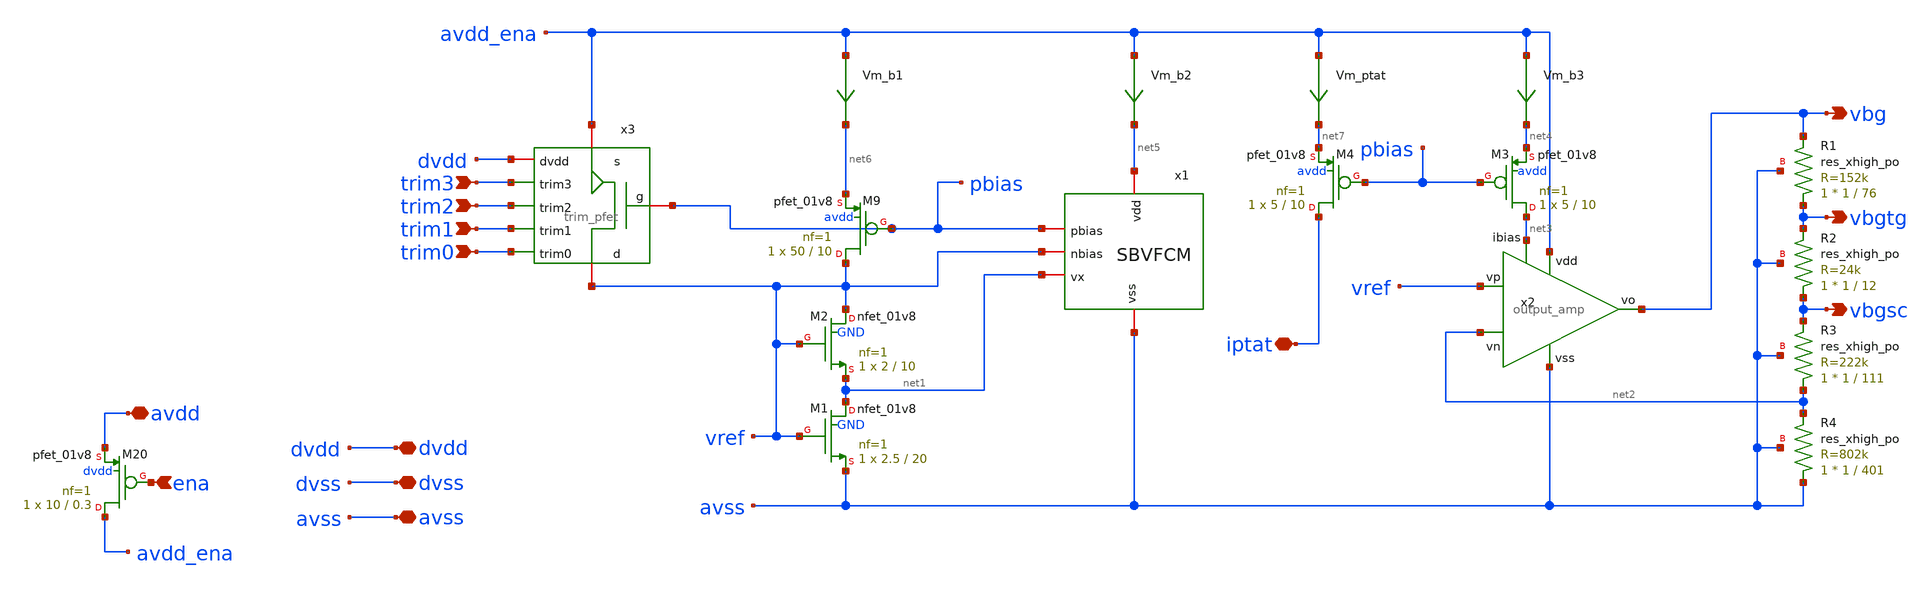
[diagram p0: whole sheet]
** sch_path: xschem/sky130_ak_ip__cmos_vref.sch
**.subckt sky130_ak_ip__cmos_vref vbg avss avdd dvdd dvss ena vbgsc vbgtg trim3 trim2 trim1 trim0
*+ iptat
*.opin vbg
*.iopin avss
*.iopin avdd
*.iopin dvdd
*.iopin dvss
*.ipin ena
*.opin vbgsc
*.opin vbgtg
*.ipin trim3
*.ipin trim2
*.ipin trim1
*.ipin trim0
*.iopin iptat
XM2 vref vref net1 GND sky130_fd_pr__nfet_01v8 L=10 W=2 nf=1 ad='int((nf+1)/2) * W/nf * 0.29' as='int((nf+2)/2) * W/nf * 0.29'
+ pd='2*int((nf+1)/2) * (W/nf + 0.29)' ps='2*int((nf+2)/2) * (W/nf + 0.29)' nrd='0.29 / W' nrs='0.29 / W'
+ sa=0 sb=0 sd=0 mult=1 m=1
XM1 net1 vref avss GND sky130_fd_pr__nfet_01v8 L=20 W=2.5 nf=1 ad='int((nf+1)/2) * W/nf * 0.29' as='int((nf+2)/2) * W/nf * 0.29'
+ pd='2*int((nf+1)/2) * (W/nf + 0.29)' ps='2*int((nf+2)/2) * (W/nf + 0.29)' nrd='0.29 / W' nrs='0.29 / W'
+ sa=0 sb=0 sd=0 mult=1 m=1
XM9 vref pbias net6 avdd sky130_fd_pr__pfet_01v8 L=10 W=50 nf=1 ad='int((nf+1)/2) * W/nf * 0.29' as='int((nf+2)/2) * W/nf * 0.29'
+ pd='2*int((nf+1)/2) * (W/nf + 0.29)' ps='2*int((nf+2)/2) * (W/nf + 0.29)' nrd='0.29 / W' nrs='0.29 / W'
+ sa=0 sb=0 sd=0 mult=1 m=1
XM20 avdd_ena ena avdd dvdd sky130_fd_pr__pfet_01v8 L=0.3 W=10 nf=1 ad='int((nf+1)/2) * W/nf * 0.29'
+ as='int((nf+2)/2) * W/nf * 0.29' pd='2*int((nf+1)/2) * (W/nf + 0.29)' ps='2*int((nf+2)/2) * (W/nf + 0.29)'
+ nrd='0.29 / W' nrs='0.29 / W' sa=0 sb=0 sd=0 mult=1 m=1
x1 net5 pbias vref net1 avss sbvfcm
x2 avdd_ena vbg vref net2 net3 avss output_amp
XM3 net3 pbias net4 avdd sky130_fd_pr__pfet_01v8 L=10 W=5 nf=1 ad='int((nf+1)/2) * W/nf * 0.29' as='int((nf+2)/2) * W/nf * 0.29'
+ pd='2*int((nf+1)/2) * (W/nf + 0.29)' ps='2*int((nf+2)/2) * (W/nf + 0.29)' nrd='0.29 / W' nrs='0.29 / W'
+ sa=0 sb=0 sd=0 mult=1 m=1
Vm_b1 avdd_ena net6 0
.save i(vm_b1)
Vm_b2 avdd_ena net5 0
.save i(vm_b2)
Vm_b3 avdd_ena net4 0
.save i(vm_b3)
x3 dvdd avdd_ena pbias trim0 trim2 trim3 trim1 vref trim_pfet
XM4 iptat pbias net7 avdd sky130_fd_pr__pfet_01v8 L=10 W=5 nf=1 ad='int((nf+1)/2) * W/nf * 0.29' as='int((nf+2)/2) * W/nf * 0.29'
+ pd='2*int((nf+1)/2) * (W/nf + 0.29)' ps='2*int((nf+2)/2) * (W/nf + 0.29)' nrd='0.29 / W' nrs='0.29 / W'
+ sa=0 sb=0 sd=0 mult=1 m=1
Vm_ptat avdd_ena net7 0
.save i(vm_ptat)
XR4 avss net2 avss sky130_fd_pr__res_xhigh_po W=1 L=401 mult=1 m=1
XR3 net2 vbgsc avss sky130_fd_pr__res_xhigh_po W=1 L=111 mult=1 m=1
XR2 vbgsc vbgtg avss sky130_fd_pr__res_xhigh_po W=1 L=12 mult=1 m=1
XR1 vbgtg vbg avss sky130_fd_pr__res_xhigh_po W=1 L=76 mult=1 m=1
**.ends

* expanding   symbol:  /home/moduhub/work/sky130_ak_ip__cmos_vref/xschem/sbvfcm.sym # of pins=5
** sym_path: xschem/sbvfcm.sym
** sch_path: xschem/sbvfcm.sch
.subckt sbvfcm vdd pbias nbias vx vss
*.iopin vss
*.iopin vdd
*.iopin vx
*.iopin pbias
*.iopin nbias
XM3 net1 vbias_st vx GND sky130_fd_pr__nfet_01v8 L=1 W=100 nf=5 ad='int((nf+1)/2) * W/nf * 0.29' as='int((nf+2)/2) * W/nf * 0.29'
+ pd='2*int((nf+1)/2) * (W/nf + 0.29)' ps='2*int((nf+2)/2) * (W/nf + 0.29)' nrd='0.29 / W' nrs='0.29 / W'
+ sa=0 sb=0 sd=0 mult=1 m=1
XM4 net2 vbias_st vss GND sky130_fd_pr__nfet_01v8 L=1 W=5 nf=1 ad='int((nf+1)/2) * W/nf * 0.29' as='int((nf+2)/2) * W/nf * 0.29'
+ pd='2*int((nf+1)/2) * (W/nf + 0.29)' ps='2*int((nf+2)/2) * (W/nf + 0.29)' nrd='0.29 / W' nrs='0.29 / W'
+ sa=0 sb=0 sd=0 mult=1 m=1
XM5 pbias nbias net1 GND sky130_fd_pr__nfet_01v8 L=10 W=10 nf=1 ad='int((nf+1)/2) * W/nf * 0.29' as='int((nf+2)/2) * W/nf * 0.29'
+ pd='2*int((nf+1)/2) * (W/nf + 0.29)' ps='2*int((nf+2)/2) * (W/nf + 0.29)' nrd='0.29 / W' nrs='0.29 / W'
+ sa=0 sb=0 sd=0 mult=1 m=1
XM6 vbias_st nbias net2 GND sky130_fd_pr__nfet_01v8 L=10 W=10 nf=1 ad='int((nf+1)/2) * W/nf * 0.29' as='int((nf+2)/2) * W/nf * 0.29'
+ pd='2*int((nf+1)/2) * (W/nf + 0.29)' ps='2*int((nf+2)/2) * (W/nf + 0.29)' nrd='0.29 / W' nrs='0.29 / W'
+ sa=0 sb=0 sd=0 mult=1 m=1
XM7 pbias pbias net5 vdd sky130_fd_pr__pfet_01v8 L=10 W=5 nf=1 ad='int((nf+1)/2) * W/nf * 0.29' as='int((nf+2)/2) * W/nf * 0.29'
+ pd='2*int((nf+1)/2) * (W/nf + 0.29)' ps='2*int((nf+2)/2) * (W/nf + 0.29)' nrd='0.29 / W' nrs='0.29 / W'
+ sa=0 sb=0 sd=0 mult=1 m=1
XM8 vbias_st pbias net6 vdd sky130_fd_pr__pfet_01v8 L=10 W=5 nf=1 ad='int((nf+1)/2) * W/nf * 0.29' as='int((nf+2)/2) * W/nf * 0.29'
+ pd='2*int((nf+1)/2) * (W/nf + 0.29)' ps='2*int((nf+2)/2) * (W/nf + 0.29)' nrd='0.29 / W' nrs='0.29 / W'
+ sa=0 sb=0 sd=0 mult=1 m=1
XM10 net3 kick vss GND sky130_fd_pr__nfet_01v8 L=10 W=5 nf=5 ad='int((nf+1)/2) * W/nf * 0.29' as='int((nf+2)/2) * W/nf * 0.29'
+ pd='2*int((nf+1)/2) * (W/nf + 0.29)' ps='2*int((nf+2)/2) * (W/nf + 0.29)' nrd='0.29 / W' nrs='0.29 / W'
+ sa=0 sb=0 sd=0 mult=1 m=1
XM11 kick vbias_st vss GND sky130_fd_pr__nfet_01v8 L=5 W=10 nf=5 ad='int((nf+1)/2) * W/nf * 0.29' as='int((nf+2)/2) * W/nf * 0.29'
+ pd='2*int((nf+1)/2) * (W/nf + 0.29)' ps='2*int((nf+2)/2) * (W/nf + 0.29)' nrd='0.29 / W' nrs='0.29 / W'
+ sa=0 sb=0 sd=0 mult=1 m=1
XC1 net4 kick sky130_fd_pr__cap_mim_m3_1 W=5 L=5 MF=1 m=1
Vm_st1 pbias net3 0
.save i(vm_st1)
Vm_st2 vdd net4 0
.save i(vm_st2)
Vm_b1 vdd net5 0
.save i(vm_b1)
Vm_b2 vdd net6 0
.save i(vm_b2)
.ends


* expanding   symbol:  /home/moduhub/work/sky130_ak_ip__cmos_vref/xschem/output_amp.sym # of pins=6
** sym_path: /home/moduhub/work/sky130_ak_ip__cmos_vref/xschem/output_amp.sym
** sch_path: /home/moduhub/work/sky130_ak_ip__cmos_vref/xschem/output_amp.sch
.subckt output_amp vdd vo vp vn ibias vss
*.ipin vp
*.ipin vn
*.ipin ibias
*.opin vo
*.ipin vss
*.ipin vdd
XM1 ibias ibias vss GND sky130_fd_pr__nfet_01v8 L=1 W=2.5 nf=1 ad='int((nf+1)/2) * W/nf * 0.29' as='int((nf+2)/2) * W/nf * 0.29'
+ pd='2*int((nf+1)/2) * (W/nf + 0.29)' ps='2*int((nf+2)/2) * (W/nf + 0.29)' nrd='0.29 / W' nrs='0.29 / W'
+ sa=0 sb=0 sd=0 mult=1 m=1
XM2 net4 ibias vss GND sky130_fd_pr__nfet_01v8 L=1 W=5 nf=1 ad='int((nf+1)/2) * W/nf * 0.29' as='int((nf+2)/2) * W/nf * 0.29'
+ pd='2*int((nf+1)/2) * (W/nf + 0.29)' ps='2*int((nf+2)/2) * (W/nf + 0.29)' nrd='0.29 / W' nrs='0.29 / W'
+ sa=0 sb=0 sd=0 mult=1 m=1
XM7 net3 net1 net6 vdd sky130_fd_pr__pfet_01v8 L=10 W=5 nf=1 ad='int((nf+1)/2) * W/nf * 0.29' as='int((nf+2)/2) * W/nf * 0.29'
+ pd='2*int((nf+1)/2) * (W/nf + 0.29)' ps='2*int((nf+2)/2) * (W/nf + 0.29)' nrd='0.29 / W' nrs='0.29 / W'
+ sa=0 sb=0 sd=0 mult=1 m=1
XM4 net9 vn net2 GND sky130_fd_pr__nfet_01v8 L=2 W=10 nf=1 ad='int((nf+1)/2) * W/nf * 0.29' as='int((nf+2)/2) * W/nf * 0.29'
+ pd='2*int((nf+1)/2) * (W/nf + 0.29)' ps='2*int((nf+2)/2) * (W/nf + 0.29)' nrd='0.29 / W' nrs='0.29 / W'
+ sa=0 sb=0 sd=0 mult=1 m=1
XM5 net10 vp net2 GND sky130_fd_pr__nfet_01v8 L=2 W=10 nf=1 ad='int((nf+1)/2) * W/nf * 0.29' as='int((nf+2)/2) * W/nf * 0.29'
+ pd='2*int((nf+1)/2) * (W/nf + 0.29)' ps='2*int((nf+2)/2) * (W/nf + 0.29)' nrd='0.29 / W' nrs='0.29 / W'
+ sa=0 sb=0 sd=0 mult=1 m=1
XM6 net1 net1 net5 vdd sky130_fd_pr__pfet_01v8 L=10 W=5 nf=1 ad='int((nf+1)/2) * W/nf * 0.29' as='int((nf+2)/2) * W/nf * 0.29'
+ pd='2*int((nf+1)/2) * (W/nf + 0.29)' ps='2*int((nf+2)/2) * (W/nf + 0.29)' nrd='0.29 / W' nrs='0.29 / W'
+ sa=0 sb=0 sd=0 mult=1 m=1
Vm_b1 vdd net5 0
.save i(vm_b1)
XM3 net8 ibias vss GND sky130_fd_pr__nfet_01v8 L=1 W=8 nf=1 ad='int((nf+1)/2) * W/nf * 0.29' as='int((nf+2)/2) * W/nf * 0.29'
+ pd='2*int((nf+1)/2) * (W/nf + 0.29)' ps='2*int((nf+2)/2) * (W/nf + 0.29)' nrd='0.29 / W' nrs='0.29 / W'
+ sa=0 sb=0 sd=0 mult=1 m=1
XM8 vo net3 net7 vdd sky130_fd_pr__pfet_01v8 L=5 W=40 nf=1 ad='int((nf+1)/2) * W/nf * 0.29' as='int((nf+2)/2) * W/nf * 0.29'
+ pd='2*int((nf+1)/2) * (W/nf + 0.29)' ps='2*int((nf+2)/2) * (W/nf + 0.29)' nrd='0.29 / W' nrs='0.29 / W'
+ sa=0 sb=0 sd=0 mult=1 m=1
Vm_op vdd net7 0
.save i(vm_op)
Vm_cm net2 net4 0
.save i(vm_cm)
Vm_b2 vdd net6 0
.save i(vm_b2)
XC2 vo net3 sky130_fd_pr__cap_mim_m3_1 W=5 L=5 MF=1 m=1
Vm_on vo net8 0
.save i(vm_on)
XM9 net1 vn net9 GND sky130_fd_pr__nfet_05v0_nvt L=2 W=20 nf=1 ad='int((nf+1)/2) * W/nf * 0.29' as='int((nf+2)/2) * W/nf * 0.29'
+ pd='2*int((nf+1)/2) * (W/nf + 0.29)' ps='2*int((nf+2)/2) * (W/nf + 0.29)' nrd='0.29 / W' nrs='0.29 / W'
+ sa=0 sb=0 sd=0 mult=1 m=1
XM10 net3 vp net10 GND sky130_fd_pr__nfet_05v0_nvt L=2 W=20 nf=1 ad='int((nf+1)/2) * W/nf * 0.29' as='int((nf+2)/2) * W/nf * 0.29'
+ pd='2*int((nf+1)/2) * (W/nf + 0.29)' ps='2*int((nf+2)/2) * (W/nf + 0.29)' nrd='0.29 / W' nrs='0.29 / W'
+ sa=0 sb=0 sd=0 mult=1 m=1
.ends


* expanding   symbol:  /home/moduhub/work/sky130_ak_ip__cmos_vref/xschem/trim_pfet.sym # of pins=8
** sym_path: xschem/trim_pfet.sym
** sch_path: xschem/trim_pfet.sch
.subckt trim_pfet dvdd source gate trim0 trim2 trim3 trim1 drain
*.ipin trim0
*.ipin trim1
*.ipin trim2
*.ipin trim3
*.iopin dvdd
*.iopin drain
*.iopin source
*.iopin gate
XM4 net4 gate source source sky130_fd_pr__pfet_01v8 L=10 W=1 nf=1 ad='int((nf+1)/2) * W/nf * 0.29' as='int((nf+2)/2) * W/nf * 0.29'
+ pd='2*int((nf+1)/2) * (W/nf + 0.29)' ps='2*int((nf+2)/2) * (W/nf + 0.29)' nrd='0.29 / W' nrs='0.29 / W'
+ sa=0 sb=0 sd=0 mult=1 m=1
XM3 net3 gate source source sky130_fd_pr__pfet_01v8 L=10 W=2 nf=1 ad='int((nf+1)/2) * W/nf * 0.29' as='int((nf+2)/2) * W/nf * 0.29'
+ pd='2*int((nf+1)/2) * (W/nf + 0.29)' ps='2*int((nf+2)/2) * (W/nf + 0.29)' nrd='0.29 / W' nrs='0.29 / W'
+ sa=0 sb=0 sd=0 mult=1 m=1
XM7 drain trim0 net4 dvdd sky130_fd_pr__pfet_01v8 L=0.15 W=1 nf=1 ad='int((nf+1)/2) * W/nf * 0.29' as='int((nf+2)/2) * W/nf * 0.29'
+ pd='2*int((nf+1)/2) * (W/nf + 0.29)' ps='2*int((nf+2)/2) * (W/nf + 0.29)' nrd='0.29 / W' nrs='0.29 / W'
+ sa=0 sb=0 sd=0 mult=1 m=1
XM6 drain trim1 net3 dvdd sky130_fd_pr__pfet_01v8 L=0.15 W=1 nf=1 ad='int((nf+1)/2) * W/nf * 0.29' as='int((nf+2)/2) * W/nf * 0.29'
+ pd='2*int((nf+1)/2) * (W/nf + 0.29)' ps='2*int((nf+2)/2) * (W/nf + 0.29)' nrd='0.29 / W' nrs='0.29 / W'
+ sa=0 sb=0 sd=0 mult=1 m=1
XM2 net5 gate net6 source sky130_fd_pr__pfet_01v8 L=10 W=4 nf=1 ad='int((nf+1)/2) * W/nf * 0.29' as='int((nf+2)/2) * W/nf * 0.29'
+ pd='2*int((nf+1)/2) * (W/nf + 0.29)' ps='2*int((nf+2)/2) * (W/nf + 0.29)' nrd='0.29 / W' nrs='0.29 / W'
+ sa=0 sb=0 sd=0 mult=1 m=1
XM5 drain trim2 net2 dvdd sky130_fd_pr__pfet_01v8 L=0.15 W=1 nf=1 ad='int((nf+1)/2) * W/nf * 0.29' as='int((nf+2)/2) * W/nf * 0.29'
+ pd='2*int((nf+1)/2) * (W/nf + 0.29)' ps='2*int((nf+2)/2) * (W/nf + 0.29)' nrd='0.29 / W' nrs='0.29 / W'
+ sa=0 sb=0 sd=0 mult=1 m=1
XM1 net1 gate source source sky130_fd_pr__pfet_01v8 L=10 W=8 nf=1 ad='int((nf+1)/2) * W/nf * 0.29' as='int((nf+2)/2) * W/nf * 0.29'
+ pd='2*int((nf+1)/2) * (W/nf + 0.29)' ps='2*int((nf+2)/2) * (W/nf + 0.29)' nrd='0.29 / W' nrs='0.29 / W'
+ sa=0 sb=0 sd=0 mult=1 m=1
XM8 drain trim3 net1 dvdd sky130_fd_pr__pfet_01v8 L=0.15 W=1 nf=1 ad='int((nf+1)/2) * W/nf * 0.29' as='int((nf+2)/2) * W/nf * 0.29'
+ pd='2*int((nf+1)/2) * (W/nf + 0.29)' ps='2*int((nf+2)/2) * (W/nf + 0.29)' nrd='0.29 / W' nrs='0.29 / W'
+ sa=0 sb=0 sd=0 mult=1 m=1
.ends

.end
